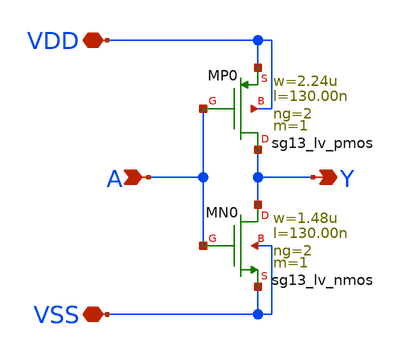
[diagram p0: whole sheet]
** sch_path: xschem/inv_2.sch
**.subckt inv_2 Y A VDD VSS
*.opin Y
*.ipin A
*.iopin VDD
*.iopin VSS
XMN0 Y A VSS VSS sg13_lv_nmos w=1.48u l=130.00n ng=2 m=1 mm_ok=1
XMP0 Y A VDD VDD sg13_lv_pmos w=2.24u l=130.00n ng=2 m=1 mm_ok=1
**.ends
.end
